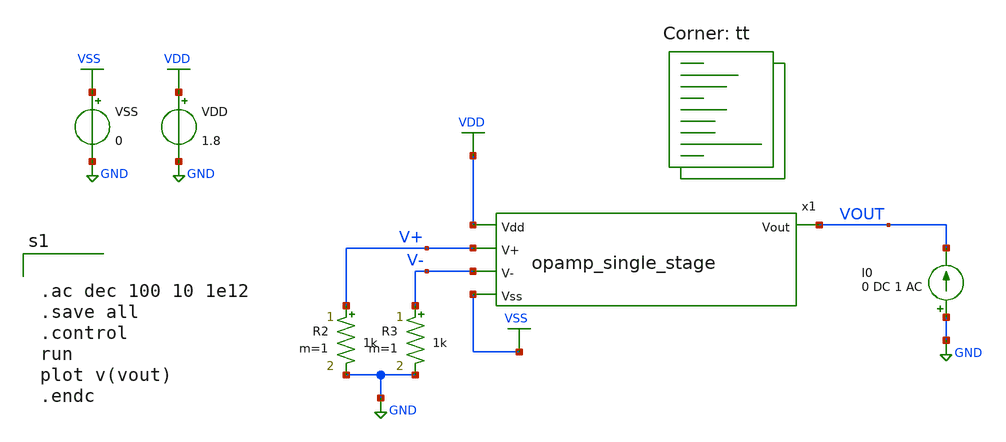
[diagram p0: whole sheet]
** sch_path: analog/schematics/tb_impedance.sch
**.subckt tb_impedance
VDD VDD GND 1.8
VSS VSS GND 0
x1 VDD VOUT V+ V- VSS opamp_single_stage
R2 V+ GND 1k m=1
R3 V- GND 1k m=1
I0 GND VOUT 0 DC 1 AC
**** begin user architecture code


.ac dec 100 10 1e12
.save all
.control
run
plot v(vout)
.endc


.lib $::SKYWATER_MODELS/sky130.lib.spice tt
**** end user architecture code
**.ends

* expanding   symbol:  opamp_single_stage.sym # of pins=5
** sym_path: analog/schematics/opamp_single_stage.sym
** sch_path: analog/schematics/opamp_single_stage.sch
.subckt opamp_single_stage Vdd Vout V+ V- Vss
*.opin Vout
*.ipin Vdd
*.ipin Vss
*.ipin V+
*.ipin V-
XM3 net1 V+ net2 Vss sky130_fd_pr__nfet_01v8 L=0.25 W=1 nf=1 ad='int((nf+1)/2) * W/nf * 0.29' as='int((nf+2)/2) * W/nf * 0.29'
+ pd='2*int((nf+1)/2) * (W/nf + 0.29)' ps='2*int((nf+2)/2) * (W/nf + 0.29)' nrd='0.29 / W' nrs='0.29 / W'
+ sa=0 sb=0 sd=0 mult=1 m=1
XM4 Vout V- net2 Vss sky130_fd_pr__nfet_01v8 L=0.25 W=1 nf=1 ad='int((nf+1)/2) * W/nf * 0.29' as='int((nf+2)/2) * W/nf * 0.29'
+ pd='2*int((nf+1)/2) * (W/nf + 0.29)' ps='2*int((nf+2)/2) * (W/nf + 0.29)' nrd='0.29 / W' nrs='0.29 / W'
+ sa=0 sb=0 sd=0 mult=1 m=1
XM5 net2 net3 Vss Vss sky130_fd_pr__nfet_01v8 L=0.25 W=1 nf=1 ad='int((nf+1)/2) * W/nf * 0.29' as='int((nf+2)/2) * W/nf * 0.29'
+ pd='2*int((nf+1)/2) * (W/nf + 0.29)' ps='2*int((nf+2)/2) * (W/nf + 0.29)' nrd='0.29 / W' nrs='0.29 / W'
+ sa=0 sb=0 sd=0 mult=1 m=1
XM1 net1 net1 Vdd Vdd sky130_fd_pr__pfet_01v8 L=0.25 W=1 nf=1 ad='int((nf+1)/2) * W/nf * 0.29' as='int((nf+2)/2) * W/nf * 0.29'
+ pd='2*int((nf+1)/2) * (W/nf + 0.29)' ps='2*int((nf+2)/2) * (W/nf + 0.29)' nrd='0.29 / W' nrs='0.29 / W'
+ sa=0 sb=0 sd=0 mult=1 m=1
XM2 Vout net1 Vdd Vdd sky130_fd_pr__pfet_01v8 L=0.25 W=1 nf=1 ad='int((nf+1)/2) * W/nf * 0.29' as='int((nf+2)/2) * W/nf * 0.29'
+ pd='2*int((nf+1)/2) * (W/nf + 0.29)' ps='2*int((nf+2)/2) * (W/nf + 0.29)' nrd='0.29 / W' nrs='0.29 / W'
+ sa=0 sb=0 sd=0 mult=1 m=1
XM6 net3 net3 Vss Vss sky130_fd_pr__nfet_01v8 L=0.25 W=1 nf=1 ad='int((nf+1)/2) * W/nf * 0.29' as='int((nf+2)/2) * W/nf * 0.29'
+ pd='2*int((nf+1)/2) * (W/nf + 0.29)' ps='2*int((nf+2)/2) * (W/nf + 0.29)' nrd='0.29 / W' nrs='0.29 / W'
+ sa=0 sb=0 sd=0 mult=1 m=1
XR1 net3 Vdd net4 sky130_fd_pr__res_high_po W=2.5 L=0.1 mult=1 m=1
.ends

.GLOBAL GND
.GLOBAL VDD
.GLOBAL VSS
.end
